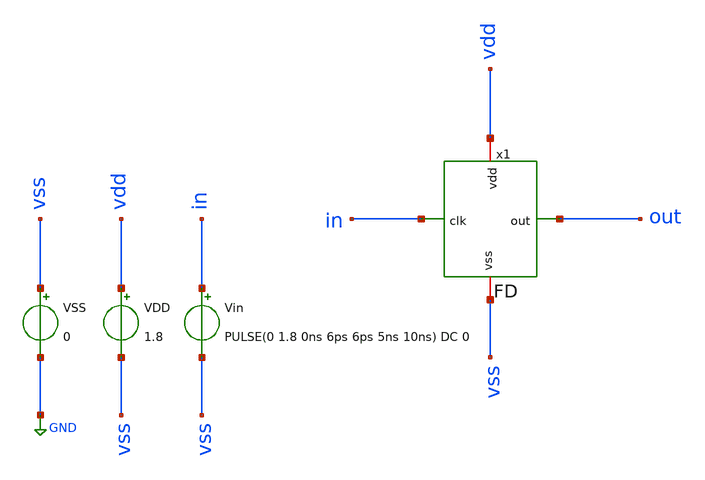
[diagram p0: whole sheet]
** sch_path: sch/PLL_caravel/tb_FD.sch
**.subckt tb_FD
VSS vss GND 0
VDD vdd vss 1.8
Vin in vss PULSE(0 1.8 0ns 6ps 6ps 5ns 10ns) DC 0
x1 in out vdd vss FD
**** begin user architecture code



* Parameters
.options TEMPS = 27.0

* Models
.lib ~/skywater/skywater-pdk/libraries/sky130_fd_pr_ngspice/latest/models/corners/sky130.lib TT

* Data to save
.save all

* Simulation
.control
	tran 0.1ns 0.2us
        setplot tran1
        plot v(in)+3 v(out)
        set filetype = ascii
        write FD_tran.raw
.endc

.end


**** end user architecture code
**.ends

* expanding   symbol:  PLL_caravel/FD.sym # of pins=4
** sym_path: sch/PLL_caravel/FD.sym
** sch_path: sch/PLL_caravel/FD.sch
.subckt FD clk out vdd vss
*.iopin vss
*.ipin clk
*.opin out
*.iopin vdd
XM1 net1 out1 vdd vdd sky130_fd_pr__pfet_01v8 L=0.15 W=0.84 nf=1 ad='int((nf+1)/2) * W/nf * 0.29' as='int((nf+2)/2) * W/nf * 0.29'
+ pd='2*int((nf+1)/2) * (W/nf + 0.29)' ps='2*int((nf+2)/2) * (W/nf + 0.29)' nrd='0.29 / W' nrs='0.29 / W'
+ sa=0 sb=0 sd=0 mult=1 m=1
XM2 net1 out1 vss vss sky130_fd_pr__nfet_01v8 L=0.15 W=0.42 nf=1 ad='int((nf+1)/2) * W/nf * 0.29' as='int((nf+2)/2) * W/nf * 0.29'
+ pd='2*int((nf+1)/2) * (W/nf + 0.29)' ps='2*int((nf+2)/2) * (W/nf + 0.29)' nrd='0.29 / W' nrs='0.29 / W'
+ sa=0 sb=0 sd=0 mult=1 m=1
XM3 net1 clkb net2 vdd sky130_fd_pr__pfet_01v8 L=0.15 W=0.84 nf=1 ad='int((nf+1)/2) * W/nf * 0.29' as='int((nf+2)/2) * W/nf * 0.29'
+ pd='2*int((nf+1)/2) * (W/nf + 0.29)' ps='2*int((nf+2)/2) * (W/nf + 0.29)' nrd='0.29 / W' nrs='0.29 / W'
+ sa=0 sb=0 sd=0 mult=1 m=1
XM4 net1 clk net2 vss sky130_fd_pr__nfet_01v8 L=0.15 W=0.42 nf=1 ad='int((nf+1)/2) * W/nf * 0.29' as='int((nf+2)/2) * W/nf * 0.29'
+ pd='2*int((nf+1)/2) * (W/nf + 0.29)' ps='2*int((nf+2)/2) * (W/nf + 0.29)' nrd='0.29 / W' nrs='0.29 / W'
+ sa=0 sb=0 sd=0 mult=1 m=1
XM5 net3 net2 vdd vdd sky130_fd_pr__pfet_01v8 L=0.15 W=0.84 nf=1 ad='int((nf+1)/2) * W/nf * 0.29' as='int((nf+2)/2) * W/nf * 0.29'
+ pd='2*int((nf+1)/2) * (W/nf + 0.29)' ps='2*int((nf+2)/2) * (W/nf + 0.29)' nrd='0.29 / W' nrs='0.29 / W'
+ sa=0 sb=0 sd=0 mult=1 m=1
XM6 net3 net2 vss vss sky130_fd_pr__nfet_01v8 L=0.15 W=0.42 nf=1 ad='int((nf+1)/2) * W/nf * 0.29' as='int((nf+2)/2) * W/nf * 0.29'
+ pd='2*int((nf+1)/2) * (W/nf + 0.29)' ps='2*int((nf+2)/2) * (W/nf + 0.29)' nrd='0.29 / W' nrs='0.29 / W'
+ sa=0 sb=0 sd=0 mult=1 m=1
XM7 net3 clk out vdd sky130_fd_pr__pfet_01v8 L=0.15 W=0.84 nf=1 ad='int((nf+1)/2) * W/nf * 0.29' as='int((nf+2)/2) * W/nf * 0.29'
+ pd='2*int((nf+1)/2) * (W/nf + 0.29)' ps='2*int((nf+2)/2) * (W/nf + 0.29)' nrd='0.29 / W' nrs='0.29 / W'
+ sa=0 sb=0 sd=0 mult=1 m=1
XM8 net3 clkb out vss sky130_fd_pr__nfet_01v8 L=0.15 W=0.42 nf=1 ad='int((nf+1)/2) * W/nf * 0.29' as='int((nf+2)/2) * W/nf * 0.29'
+ pd='2*int((nf+1)/2) * (W/nf + 0.29)' ps='2*int((nf+2)/2) * (W/nf + 0.29)' nrd='0.29 / W' nrs='0.29 / W'
+ sa=0 sb=0 sd=0 mult=1 m=1
XM9 out1 out vdd vdd sky130_fd_pr__pfet_01v8 L=0.15 W=0.84 nf=1 ad='int((nf+1)/2) * W/nf * 0.29' as='int((nf+2)/2) * W/nf * 0.29'
+ pd='2*int((nf+1)/2) * (W/nf + 0.29)' ps='2*int((nf+2)/2) * (W/nf + 0.29)' nrd='0.29 / W' nrs='0.29 / W'
+ sa=0 sb=0 sd=0 mult=1 m=1
XM10 out1 out vss vss sky130_fd_pr__nfet_01v8 L=0.15 W=0.42 nf=1 ad='int((nf+1)/2) * W/nf * 0.29' as='int((nf+2)/2) * W/nf * 0.29'
+ pd='2*int((nf+1)/2) * (W/nf + 0.29)' ps='2*int((nf+2)/2) * (W/nf + 0.29)' nrd='0.29 / W' nrs='0.29 / W'
+ sa=0 sb=0 sd=0 mult=1 m=1
XM11 clkb clk vdd vdd sky130_fd_pr__pfet_01v8 L=0.15 W=0.84 nf=1 ad='int((nf+1)/2) * W/nf * 0.29' as='int((nf+2)/2) * W/nf * 0.29'
+ pd='2*int((nf+1)/2) * (W/nf + 0.29)' ps='2*int((nf+2)/2) * (W/nf + 0.29)' nrd='0.29 / W' nrs='0.29 / W'
+ sa=0 sb=0 sd=0 mult=1 m=1
XM12 clkb clk vss vss sky130_fd_pr__nfet_01v8 L=0.15 W=0.42 nf=1 ad='int((nf+1)/2) * W/nf * 0.29' as='int((nf+2)/2) * W/nf * 0.29'
+ pd='2*int((nf+1)/2) * (W/nf + 0.29)' ps='2*int((nf+2)/2) * (W/nf + 0.29)' nrd='0.29 / W' nrs='0.29 / W'
+ sa=0 sb=0 sd=0 mult=1 m=1
.ends

.GLOBAL GND
.end
